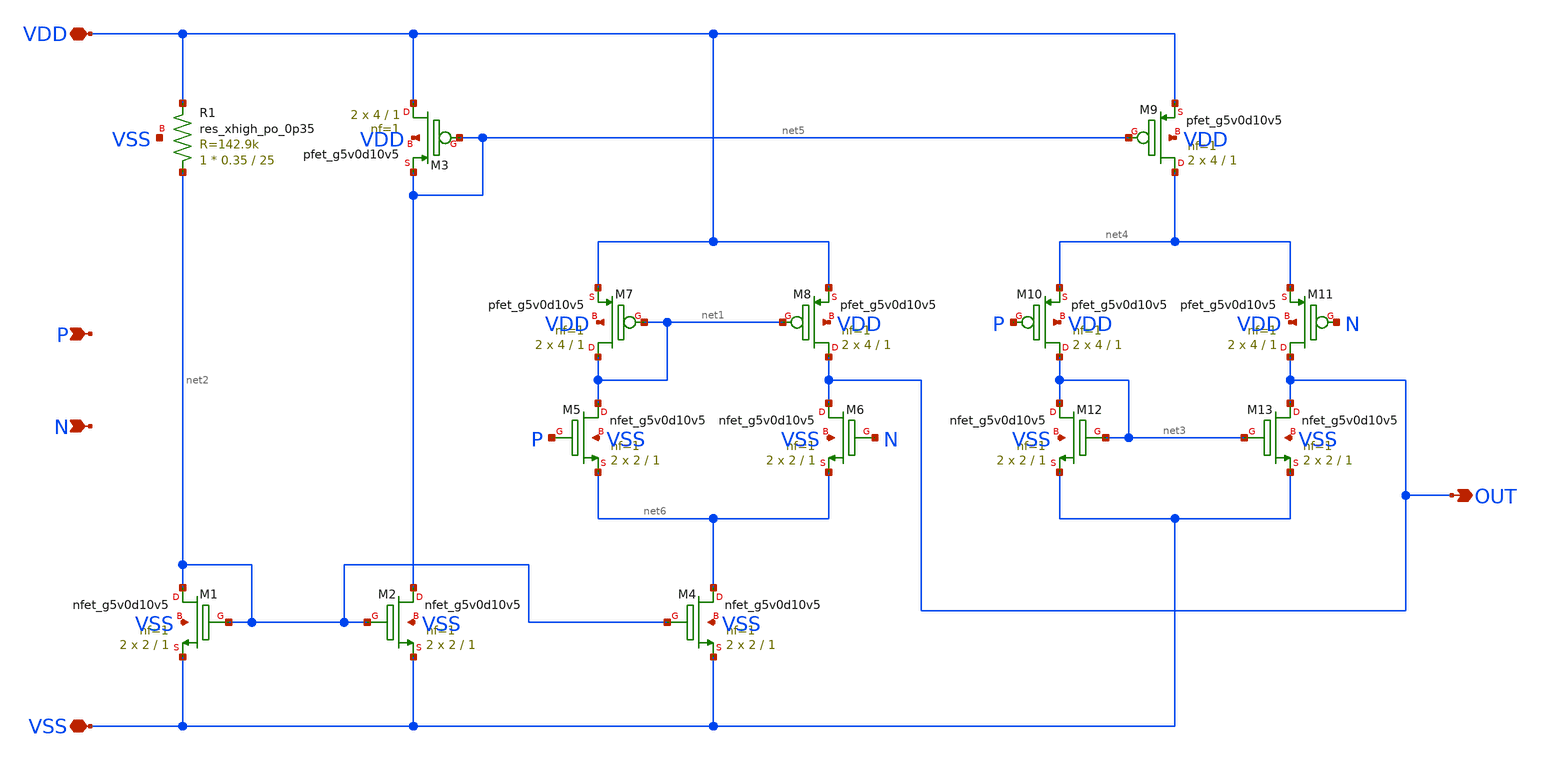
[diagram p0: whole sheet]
** sch_path: xschem/opamp.sch
**.subckt opamp VDD VSS P N OUT
*.iopin VDD
*.iopin VSS
*.ipin P
*.ipin N
*.opin OUT
XR1 net2 VDD VSS sky130_fd_pr__res_xhigh_po_0p35 L=25 mult=1 m=1
XM1 net2 net2 VSS VSS sky130_fd_pr__nfet_g5v0d10v5 L=1 W=2 nf=1 ad='int((1 + 1)/2) * 2 / 1 * 0.29' as='int((1 + 2)/2) * 2 / 1 * 0.29'
+ pd='2*int((1 + 1)/2) * (2 / 1 + 0.29)' ps='2*int((1 + 2)/2) * (2 / 1 + 0.29)' nrd='0.29 / 2 ' nrs='0.29 / 2 '
+ sa=0 sb=0 sd=0 mult=2 m=2
XM7 net1 net1 VDD VDD sky130_fd_pr__pfet_g5v0d10v5 L=1 W=4 nf=1 ad='int((1 + 1)/2) * 4 / 1 * 0.29' as='int((1 + 2)/2) * 4 / 1 * 0.29'
+ pd='2*int((1 + 1)/2) * (4 / 1 + 0.29)' ps='2*int((1 + 2)/2) * (4 / 1 + 0.29)' nrd='0.29 / 4 ' nrs='0.29 / 4 '
+ sa=0 sb=0 sd=0 mult=2 m=2
XM8 OUT net1 VDD VDD sky130_fd_pr__pfet_g5v0d10v5 L=1 W=4 nf=1 ad='int((1 + 1)/2) * 4 / 1 * 0.29' as='int((1 + 2)/2) * 4 / 1 * 0.29'
+ pd='2*int((1 + 1)/2) * (4 / 1 + 0.29)' ps='2*int((1 + 2)/2) * (4 / 1 + 0.29)' nrd='0.29 / 4 ' nrs='0.29 / 4 '
+ sa=0 sb=0 sd=0 mult=2 m=2
XM4 net6 net2 VSS VSS sky130_fd_pr__nfet_g5v0d10v5 L=1 W=2 nf=1 ad='int((1 + 1)/2) * 2 / 1 * 0.29' as='int((1 + 2)/2) * 2 / 1 * 0.29'
+ pd='2*int((1 + 1)/2) * (2 / 1 + 0.29)' ps='2*int((1 + 2)/2) * (2 / 1 + 0.29)' nrd='0.29 / 2 ' nrs='0.29 / 2 '
+ sa=0 sb=0 sd=0 mult=2 m=2
XM5 net1 P net6 VSS sky130_fd_pr__nfet_g5v0d10v5 L=1 W=2 nf=1 ad='int((1 + 1)/2) * 2 / 1 * 0.29' as='int((1 + 2)/2) * 2 / 1 * 0.29'
+ pd='2*int((1 + 1)/2) * (2 / 1 + 0.29)' ps='2*int((1 + 2)/2) * (2 / 1 + 0.29)' nrd='0.29 / 2 ' nrs='0.29 / 2 '
+ sa=0 sb=0 sd=0 mult=2 m=2
XM6 OUT N net6 VSS sky130_fd_pr__nfet_g5v0d10v5 L=1 W=2 nf=1 ad='int((1 + 1)/2) * 2 / 1 * 0.29' as='int((1 + 2)/2) * 2 / 1 * 0.29'
+ pd='2*int((1 + 1)/2) * (2 / 1 + 0.29)' ps='2*int((1 + 2)/2) * (2 / 1 + 0.29)' nrd='0.29 / 2 ' nrs='0.29 / 2 '
+ sa=0 sb=0 sd=0 mult=2 m=2
XM2 net5 net2 VSS VSS sky130_fd_pr__nfet_g5v0d10v5 L=1 W=2 nf=1 ad='int((1 + 1)/2) * 2 / 1 * 0.29' as='int((1 + 2)/2) * 2 / 1 * 0.29'
+ pd='2*int((1 + 1)/2) * (2 / 1 + 0.29)' ps='2*int((1 + 2)/2) * (2 / 1 + 0.29)' nrd='0.29 / 2 ' nrs='0.29 / 2 '
+ sa=0 sb=0 sd=0 mult=2 m=2
XM9 net4 net5 VDD VDD sky130_fd_pr__pfet_g5v0d10v5 L=1 W=4 nf=1 ad='int((1 + 1)/2) * 4 / 1 * 0.29' as='int((1 + 2)/2) * 4 / 1 * 0.29'
+ pd='2*int((1 + 1)/2) * (4 / 1 + 0.29)' ps='2*int((1 + 2)/2) * (4 / 1 + 0.29)' nrd='0.29 / 4 ' nrs='0.29 / 4 '
+ sa=0 sb=0 sd=0 mult=2 m=2
XM3 VDD net5 net5 VDD sky130_fd_pr__pfet_g5v0d10v5 L=1 W=4 nf=1 ad='int((1 + 1)/2) * 4 / 1 * 0.29' as='int((1 + 2)/2) * 4 / 1 * 0.29'
+ pd='2*int((1 + 1)/2) * (4 / 1 + 0.29)' ps='2*int((1 + 2)/2) * (4 / 1 + 0.29)' nrd='0.29 / 4 ' nrs='0.29 / 4 '
+ sa=0 sb=0 sd=0 mult=2 m=2
XM10 net3 P net4 VDD sky130_fd_pr__pfet_g5v0d10v5 L=1 W=4 nf=1 ad='int((1 + 1)/2) * 4 / 1 * 0.29' as='int((1 + 2)/2) * 4 / 1 * 0.29'
+ pd='2*int((1 + 1)/2) * (4 / 1 + 0.29)' ps='2*int((1 + 2)/2) * (4 / 1 + 0.29)' nrd='0.29 / 4 ' nrs='0.29 / 4 '
+ sa=0 sb=0 sd=0 mult=2 m=2
XM11 OUT N net4 VDD sky130_fd_pr__pfet_g5v0d10v5 L=1 W=4 nf=1 ad='int((1 + 1)/2) * 4 / 1 * 0.29' as='int((1 + 2)/2) * 4 / 1 * 0.29'
+ pd='2*int((1 + 1)/2) * (4 / 1 + 0.29)' ps='2*int((1 + 2)/2) * (4 / 1 + 0.29)' nrd='0.29 / 4 ' nrs='0.29 / 4 '
+ sa=0 sb=0 sd=0 mult=2 m=2
XM12 net3 net3 VSS VSS sky130_fd_pr__nfet_g5v0d10v5 L=1 W=2 nf=1 ad='int((1 + 1)/2) * 2 / 1 * 0.29' as='int((1 + 2)/2) * 2 / 1 * 0.29'
+ pd='2*int((1 + 1)/2) * (2 / 1 + 0.29)' ps='2*int((1 + 2)/2) * (2 / 1 + 0.29)' nrd='0.29 / 2 ' nrs='0.29 / 2 '
+ sa=0 sb=0 sd=0 mult=2 m=2
XM13 OUT net3 VSS VSS sky130_fd_pr__nfet_g5v0d10v5 L=1 W=2 nf=1 ad='int((1 + 1)/2) * 2 / 1 * 0.29' as='int((1 + 2)/2) * 2 / 1 * 0.29'
+ pd='2*int((1 + 1)/2) * (2 / 1 + 0.29)' ps='2*int((1 + 2)/2) * (2 / 1 + 0.29)' nrd='0.29 / 2 ' nrs='0.29 / 2 '
+ sa=0 sb=0 sd=0 mult=2 m=2
**.ends
.end
